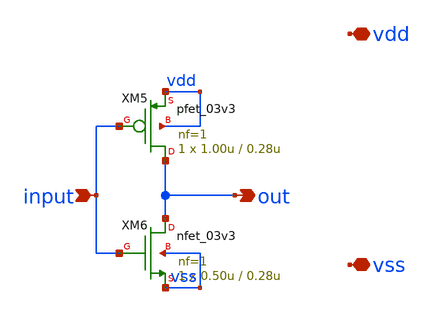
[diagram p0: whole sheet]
** sch_path: xschem/sar_adc/blocks/async_sar/async_inverter.sch
**.subckt async_inverter input out vdd vss
*.ipin input
*.opin out
*.iopin vdd
*.iopin vss
XM5 out input vdd vdd pfet_03v3 L=0.28u W=1.00u nf=1 ad='int((nf+1)/2) * W/nf * 0.18u' as='int((nf+2)/2) * W/nf * 0.18u'
+ pd='2*int((nf+1)/2) * (W/nf + 0.18u)' ps='2*int((nf+2)/2) * (W/nf + 0.18u)' nrd='0.18u / W' nrs='0.18u / W'
+ sa=0 sb=0 sd=0 m=1
XM6 out input vss vss nfet_03v3 L=0.28u W=0.50u nf=1 ad='int((nf+1)/2) * W/nf * 0.18u' as='int((nf+2)/2) * W/nf * 0.18u'
+ pd='2*int((nf+1)/2) * (W/nf + 0.18u)' ps='2*int((nf+2)/2) * (W/nf + 0.18u)' nrd='0.18u / W' nrs='0.18u / W'
+ sa=0 sb=0 sd=0 m=1
**.ends
.end
